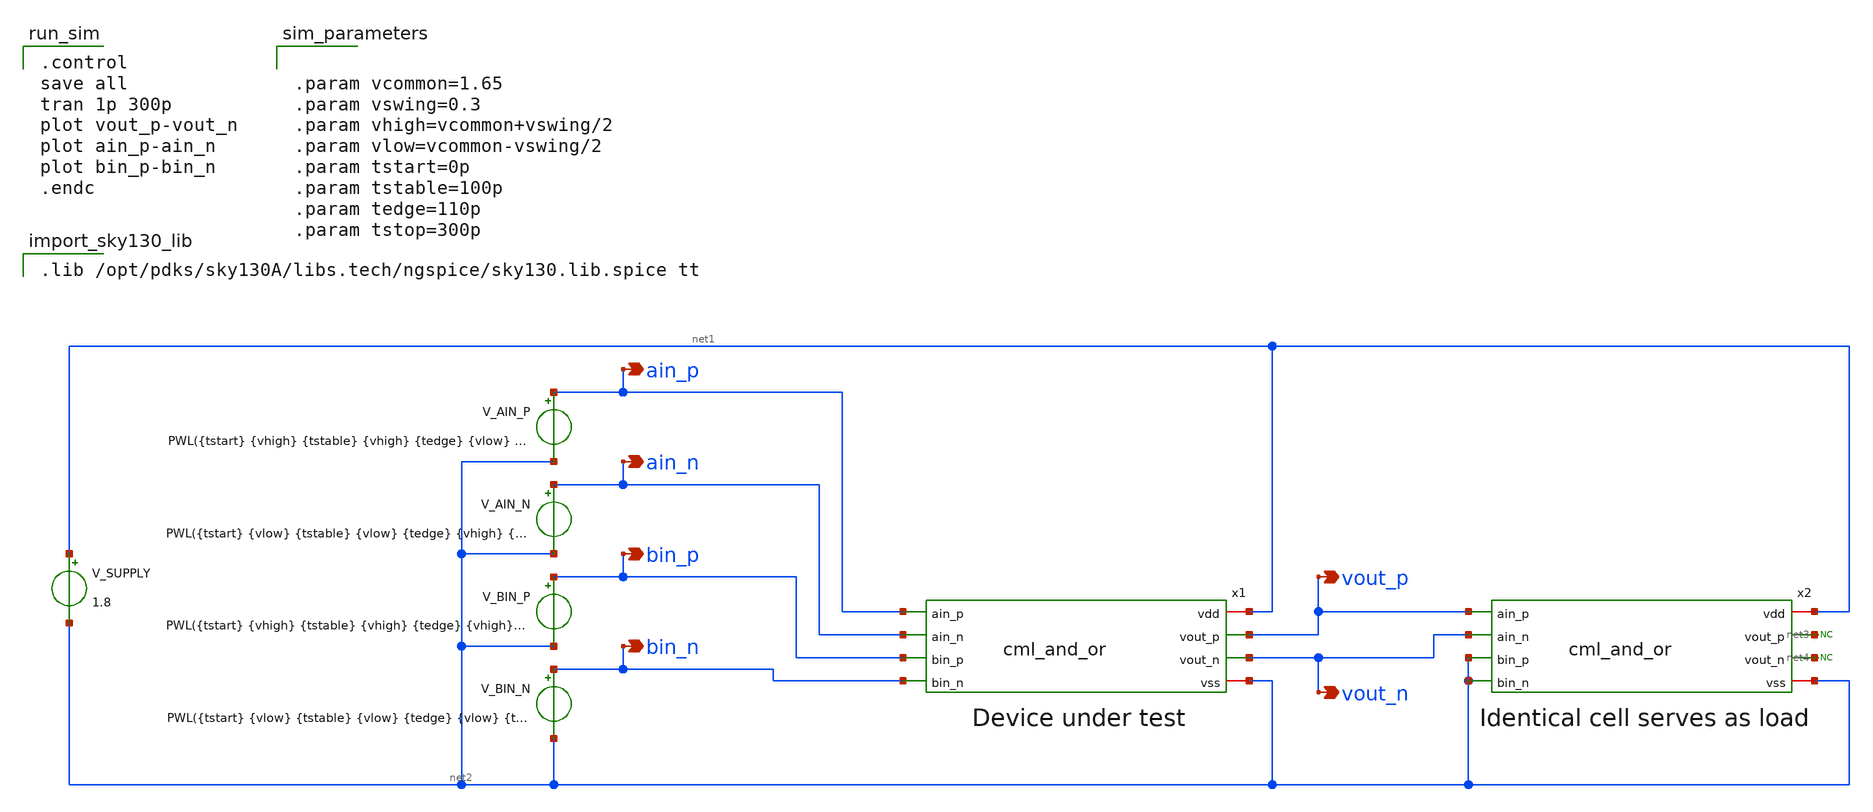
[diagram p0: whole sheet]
** sch_path: xschem/cml_and_or_tb.sch
**.subckt cml_and_or_tb vout_n vout_p ain_p ain_n bin_p bin_n
*.opin vout_n
*.opin vout_p
*.opin ain_p
*.opin ain_n
*.opin bin_p
*.opin bin_n
V_SUPPLY net1 net2 1.8
* noconn #net3
* noconn #net4
V_AIN_P ain_p net2 PWL({tstart} {vhigh} {tstable} {vhigh} {tedge} {vlow} {tstop} {vlow})
V_AIN_N ain_n net2 PWL({tstart} {vlow} {tstable} {vlow} {tedge} {vhigh} {tstop} {vhigh})
V_BIN_P bin_p net2 PWL({tstart} {vhigh} {tstable} {vhigh} {tedge} {vhigh} {tstop} {vhigh})
V_BIN_N bin_n net2 PWL({tstart} {vlow} {tstable} {vlow} {tedge} {vlow} {tstop} {vlow})
x1 net1 vout_p vout_n ain_p ain_n bin_p bin_n net2 cml_and_or
x2 net1 net3 net4 vout_p vout_n net2 net2 net2 cml_and_or
**** begin user architecture code

.lib /opt/pdks/sky130A/libs.tech/ngspice/sky130.lib.spice tt


.control
save all
tran 1p 300p
plot vout_p-vout_n
plot ain_p-ain_n
plot bin_p-bin_n
.endc



.param vcommon=1.65
.param vswing=0.3
.param vhigh=vcommon+vswing/2
.param vlow=vcommon-vswing/2
.param tstart=0p
.param tstable=100p
.param tedge=110p
.param tstop=300p


**** end user architecture code
**.ends

* expanding   symbol:  cml_and_or.sym # of pins=8
** sym_path: xschem/cml_and_or.sym
** sch_path: xschem/cml_and_or.sch
.subckt cml_and_or vdd vout_p vout_n ain_p ain_n bin_p bin_n vss
*.ipin ain_p
*.ipin ain_n
*.ipin bin_n
*.ipin bin_p
*.opin vout_p
*.opin vout_n
*.iopin vdd
*.iopin vss
XM1 vout_n ain_p net1 vss sky130_fd_pr__nfet_01v8 L=0.15 W=40 nf=1 ad='int((nf+1)/2) * W/nf * 0.29' as='int((nf+2)/2) * W/nf * 0.29'
+ pd='2*int((nf+1)/2) * (W/nf + 0.29)' ps='2*int((nf+2)/2) * (W/nf + 0.29)' nrd='0.29 / W' nrs='0.29 / W'
+ sa=0 sb=0 sd=0 mult=1 m=1
XM2 vout_p ain_n net1 vss sky130_fd_pr__nfet_01v8 L=0.15 W=40 nf=1 ad='int((nf+1)/2) * W/nf * 0.29' as='int((nf+2)/2) * W/nf * 0.29'
+ pd='2*int((nf+1)/2) * (W/nf + 0.29)' ps='2*int((nf+2)/2) * (W/nf + 0.29)' nrd='0.29 / W' nrs='0.29 / W'
+ sa=0 sb=0 sd=0 mult=1 m=1
XM3 net1 bin_p net2 vss sky130_fd_pr__nfet_01v8 L=0.15 W=40 nf=1 ad='int((nf+1)/2) * W/nf * 0.29' as='int((nf+2)/2) * W/nf * 0.29'
+ pd='2*int((nf+1)/2) * (W/nf + 0.29)' ps='2*int((nf+2)/2) * (W/nf + 0.29)' nrd='0.29 / W' nrs='0.29 / W'
+ sa=0 sb=0 sd=0 mult=1 m=1
XM4 vout_p bin_n net2 vss sky130_fd_pr__nfet_01v8 L=0.15 W=40 nf=1 ad='int((nf+1)/2) * W/nf * 0.29' as='int((nf+2)/2) * W/nf * 0.29'
+ pd='2*int((nf+1)/2) * (W/nf + 0.29)' ps='2*int((nf+2)/2) * (W/nf + 0.29)' nrd='0.29 / W' nrs='0.29 / W'
+ sa=0 sb=0 sd=0 mult=1 m=1
R1 vdd vout_n 300 m=1
R2 vdd vout_p 300 m=1
I0 net2 vss 1m
.ends

.end
